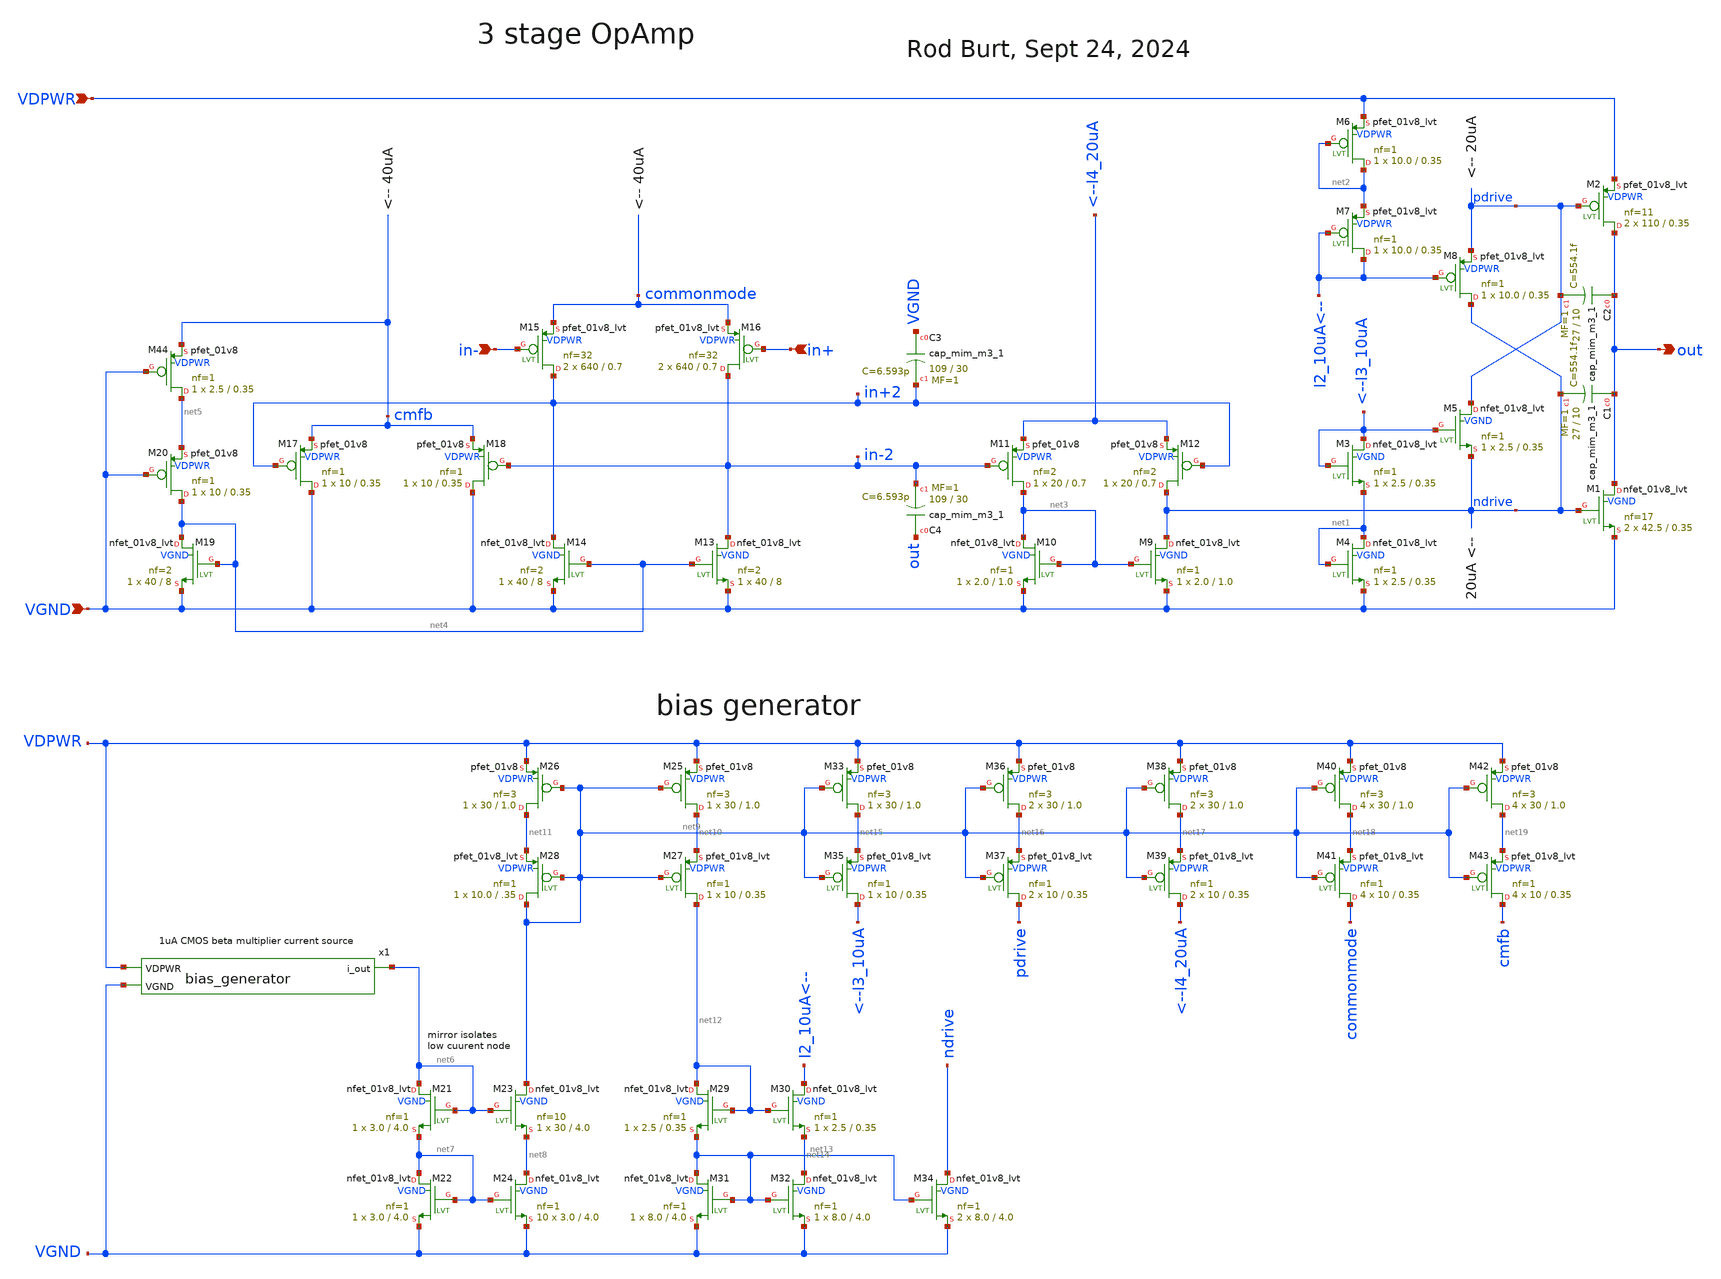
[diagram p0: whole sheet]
** sch_path: xschem/op_amp_3stage.sch
**.subckt op_amp_3stage out VDPWR VGND in- in+
*.opin out
*.ipin VDPWR
*.ipin VGND
*.ipin in-
*.ipin in+
XM2 out pdrive VDPWR VDPWR sky130_fd_pr__pfet_01v8_lvt L=0.35 W=110 nf=11 ad='int((nf+1)/2) * W/nf * 0.29'
+ as='int((nf+2)/2) * W/nf * 0.29' pd='2*int((nf+1)/2) * (W/nf + 0.29)' ps='2*int((nf+2)/2) * (W/nf + 0.29)'
+ nrd='0.29 / W' nrs='0.29 / W' sa=0 sb=0 sd=0 mult=2 m=2
XM6 net2 net2 VDPWR VDPWR sky130_fd_pr__pfet_01v8_lvt L=0.35 W=10.0 nf=1 ad='int((nf+1)/2) * W/nf * 0.29'
+ as='int((nf+2)/2) * W/nf * 0.29' pd='2*int((nf+1)/2) * (W/nf + 0.29)' ps='2*int((nf+2)/2) * (W/nf + 0.29)'
+ nrd='0.29 / W' nrs='0.29 / W' sa=0 sb=0 sd=0 mult=1 m=1
XM8 ndrive I2_10uA<-- pdrive VDPWR sky130_fd_pr__pfet_01v8_lvt L=0.35 W=10.0 nf=1 ad='int((nf+1)/2) * W/nf * 0.29'
+ as='int((nf+2)/2) * W/nf * 0.29' pd='2*int((nf+1)/2) * (W/nf + 0.29)' ps='2*int((nf+2)/2) * (W/nf + 0.29)'
+ nrd='0.29 / W' nrs='0.29 / W' sa=0 sb=0 sd=0 mult=1 m=1
XM7 I2_10uA<-- I2_10uA<-- net2 VDPWR sky130_fd_pr__pfet_01v8_lvt L=0.35 W=10.0 nf=1 ad='int((nf+1)/2) * W/nf * 0.29'
+ as='int((nf+2)/2) * W/nf * 0.29' pd='2*int((nf+1)/2) * (W/nf + 0.29)' ps='2*int((nf+2)/2) * (W/nf + 0.29)'
+ nrd='0.29 / W' nrs='0.29 / W' sa=0 sb=0 sd=0 mult=1 m=1
XM3 <--I3_10uA <--I3_10uA net1 VGND sky130_fd_pr__nfet_01v8_lvt L=0.35 W=2.5 nf=1 ad='int((nf+1)/2) * W/nf * 0.29'
+ as='int((nf+2)/2) * W/nf * 0.29' pd='2*int((nf+1)/2) * (W/nf + 0.29)' ps='2*int((nf+2)/2) * (W/nf + 0.29)'
+ nrd='0.29 / W' nrs='0.29 / W' sa=0 sb=0 sd=0 mult=1 m=1
M5 pdrive <--I3_10uA ndrive VGND sky130_fd_pr__nfet_01v8_lvt L=0.35 W=2.5 nf=1 ad='int((nf+1)/2) * W/nf * 0.29'
+ as='int((nf+2)/2) * W/nf * 0.29' pd='2*int((nf+1)/2) * (W/nf + 0.29)' ps='2*int((nf+2)/2) * (W/nf + 0.29)'
+ nrd='0.29 / W' nrs='0.29 / W' sa=0 sb=0 sd=0 mult=1 m=1
XM4 net1 net1 VGND VGND sky130_fd_pr__nfet_01v8_lvt L=0.35 W=2.5 nf=1 ad='int((nf+1)/2) * W/nf * 0.29'
+ as='int((nf+2)/2) * W/nf * 0.29' pd='2*int((nf+1)/2) * (W/nf + 0.29)' ps='2*int((nf+2)/2) * (W/nf + 0.29)'
+ nrd='0.29 / W' nrs='0.29 / W' sa=0 sb=0 sd=0 mult=1 m=1
XM1 out ndrive VGND VGND sky130_fd_pr__nfet_01v8_lvt L=0.35 W=42.5 nf=17 ad='int((nf+1)/2) * W/nf * 0.29'
+ as='int((nf+2)/2) * W/nf * 0.29' pd='2*int((nf+1)/2) * (W/nf + 0.29)' ps='2*int((nf+2)/2) * (W/nf + 0.29)'
+ nrd='0.29 / W' nrs='0.29 / W' sa=0 sb=0 sd=0 mult=2 m=2
XM9 ndrive net3 VGND VGND sky130_fd_pr__nfet_01v8_lvt L=1.0 W=2.0 nf=1 ad='int((nf+1)/2) * W/nf * 0.29'
+ as='int((nf+2)/2) * W/nf * 0.29' pd='2*int((nf+1)/2) * (W/nf + 0.29)' ps='2*int((nf+2)/2) * (W/nf + 0.29)'
+ nrd='0.29 / W' nrs='0.29 / W' sa=0 sb=0 sd=0 mult=1 m=1
XM10 net3 net3 VGND VGND sky130_fd_pr__nfet_01v8_lvt L=1.0 W=2.0 nf=1 ad='int((nf+1)/2) * W/nf * 0.29'
+ as='int((nf+2)/2) * W/nf * 0.29' pd='2*int((nf+1)/2) * (W/nf + 0.29)' ps='2*int((nf+2)/2) * (W/nf + 0.29)'
+ nrd='0.29 / W' nrs='0.29 / W' sa=0 sb=0 sd=0 mult=1 m=1
XM11 net3 in-2 <--I4_20uA VDPWR sky130_fd_pr__pfet_01v8 L=0.7 W=20 nf=2 ad='int((nf+1)/2) * W/nf * 0.29'
+ as='int((nf+2)/2) * W/nf * 0.29' pd='2*int((nf+1)/2) * (W/nf + 0.29)' ps='2*int((nf+2)/2) * (W/nf + 0.29)'
+ nrd='0.29 / W' nrs='0.29 / W' sa=0 sb=0 sd=0 mult=1 m=1
XM12 ndrive in+2 <--I4_20uA VDPWR sky130_fd_pr__pfet_01v8 L=0.7 W=20 nf=2 ad='int((nf+1)/2) * W/nf * 0.29'
+ as='int((nf+2)/2) * W/nf * 0.29' pd='2*int((nf+1)/2) * (W/nf + 0.29)' ps='2*int((nf+2)/2) * (W/nf + 0.29)'
+ nrd='0.29 / W' nrs='0.29 / W' sa=0 sb=0 sd=0 mult=1 m=1
XC1 out ndrive sky130_fd_pr__cap_mim_m3_1 W=27 L=10 MF=1 m=1
XC2 out pdrive sky130_fd_pr__cap_mim_m3_1 W=27 L=10 MF=1 m=1
XM13 in-2 net4 VGND VGND sky130_fd_pr__nfet_01v8_lvt L=8 W=40 nf=2 ad='int((nf+1)/2) * W/nf * 0.29' as='int((nf+2)/2) * W/nf * 0.29'
+ pd='2*int((nf+1)/2) * (W/nf + 0.29)' ps='2*int((nf+2)/2) * (W/nf + 0.29)' nrd='0.29 / W' nrs='0.29 / W'
+ sa=0 sb=0 sd=0 mult=1 m=1
XM14 in+2 net4 VGND VGND sky130_fd_pr__nfet_01v8_lvt L=8 W=40 nf=2 ad='int((nf+1)/2) * W/nf * 0.29' as='int((nf+2)/2) * W/nf * 0.29'
+ pd='2*int((nf+1)/2) * (W/nf + 0.29)' ps='2*int((nf+2)/2) * (W/nf + 0.29)' nrd='0.29 / W' nrs='0.29 / W'
+ sa=0 sb=0 sd=0 mult=1 m=1
XC3 VGND in+2 sky130_fd_pr__cap_mim_m3_1 W=109 L=30 MF=1 m=1
XC4 out in-2 sky130_fd_pr__cap_mim_m3_1 W=109 L=30 MF=1 m=1
XM15 in+2 in- commonmode VDPWR sky130_fd_pr__pfet_01v8_lvt L=0.7 W=640 nf=32 ad='int((nf+1)/2) * W/nf * 0.29'
+ as='int((nf+2)/2) * W/nf * 0.29' pd='2*int((nf+1)/2) * (W/nf + 0.29)' ps='2*int((nf+2)/2) * (W/nf + 0.29)'
+ nrd='0.29 / W' nrs='0.29 / W' sa=0 sb=0 sd=0 mult=2 m=2
XM16 in-2 in+ commonmode VDPWR sky130_fd_pr__pfet_01v8_lvt L=0.7 W=640 nf=32 ad='int((nf+1)/2) * W/nf * 0.29'
+ as='int((nf+2)/2) * W/nf * 0.29' pd='2*int((nf+1)/2) * (W/nf + 0.29)' ps='2*int((nf+2)/2) * (W/nf + 0.29)'
+ nrd='0.29 / W' nrs='0.29 / W' sa=0 sb=0 sd=0 mult=2 m=2
XM19 net4 net4 VGND VGND sky130_fd_pr__nfet_01v8_lvt L=8 W=40 nf=2 ad='int((nf+1)/2) * W/nf * 0.29' as='int((nf+2)/2) * W/nf * 0.29'
+ pd='2*int((nf+1)/2) * (W/nf + 0.29)' ps='2*int((nf+2)/2) * (W/nf + 0.29)' nrd='0.29 / W' nrs='0.29 / W'
+ sa=0 sb=0 sd=0 mult=1 m=1
XM20 net4 VGND net5 VDPWR sky130_fd_pr__pfet_01v8 L=0.35 W=10 nf=1 ad='int((nf+1)/2) * W/nf * 0.29' as='int((nf+2)/2) * W/nf * 0.29'
+ pd='2*int((nf+1)/2) * (W/nf + 0.29)' ps='2*int((nf+2)/2) * (W/nf + 0.29)' nrd='0.29 / W' nrs='0.29 / W'
+ sa=0 sb=0 sd=0 mult=1 m=1
XM17 VGND in+2 cmfb VDPWR sky130_fd_pr__pfet_01v8 L=0.35 W=10 nf=1 ad='int((nf+1)/2) * W/nf * 0.29' as='int((nf+2)/2) * W/nf * 0.29'
+ pd='2*int((nf+1)/2) * (W/nf + 0.29)' ps='2*int((nf+2)/2) * (W/nf + 0.29)' nrd='0.29 / W' nrs='0.29 / W'
+ sa=0 sb=0 sd=0 mult=1 m=1
XM18 VGND in-2 cmfb VDPWR sky130_fd_pr__pfet_01v8 L=0.35 W=10 nf=1 ad='int((nf+1)/2) * W/nf * 0.29' as='int((nf+2)/2) * W/nf * 0.29'
+ pd='2*int((nf+1)/2) * (W/nf + 0.29)' ps='2*int((nf+2)/2) * (W/nf + 0.29)' nrd='0.29 / W' nrs='0.29 / W'
+ sa=0 sb=0 sd=0 mult=1 m=1
x1 VDPWR net6 VGND bias_generator
XM21 net6 net6 net7 VGND sky130_fd_pr__nfet_01v8_lvt L=4.0 W=3.0 nf=1 ad='int((nf+1)/2) * W/nf * 0.29'
+ as='int((nf+2)/2) * W/nf * 0.29' pd='2*int((nf+1)/2) * (W/nf + 0.29)' ps='2*int((nf+2)/2) * (W/nf + 0.29)'
+ nrd='0.29 / W' nrs='0.29 / W' sa=0 sb=0 sd=0 mult=1 m=1
XM23 net9 net6 net8 VGND sky130_fd_pr__nfet_01v8_lvt L=4.0 W=30 nf=10 ad='int((nf+1)/2) * W/nf * 0.29'
+ as='int((nf+2)/2) * W/nf * 0.29' pd='2*int((nf+1)/2) * (W/nf + 0.29)' ps='2*int((nf+2)/2) * (W/nf + 0.29)'
+ nrd='0.29 / W' nrs='0.29 / W' sa=0 sb=0 sd=0 mult=1 m=1
XM25 net10 net9 VDPWR VDPWR sky130_fd_pr__pfet_01v8 L=1.0 W=30 nf=3 ad='int((nf+1)/2) * W/nf * 0.29'
+ as='int((nf+2)/2) * W/nf * 0.29' pd='2*int((nf+1)/2) * (W/nf + 0.29)' ps='2*int((nf+2)/2) * (W/nf + 0.29)'
+ nrd='0.29 / W' nrs='0.29 / W' sa=0 sb=0 sd=0 mult=1 m=1
XM26 net11 net9 VDPWR VDPWR sky130_fd_pr__pfet_01v8 L=1.0 W=30 nf=3 ad='int((nf+1)/2) * W/nf * 0.29'
+ as='int((nf+2)/2) * W/nf * 0.29' pd='2*int((nf+1)/2) * (W/nf + 0.29)' ps='2*int((nf+2)/2) * (W/nf + 0.29)'
+ nrd='0.29 / W' nrs='0.29 / W' sa=0 sb=0 sd=0 mult=1 m=1
XM27 net12 net9 net10 VDPWR sky130_fd_pr__pfet_01v8_lvt L=0.35 W=10 nf=1 ad='int((nf+1)/2) * W/nf * 0.29'
+ as='int((nf+2)/2) * W/nf * 0.29' pd='2*int((nf+1)/2) * (W/nf + 0.29)' ps='2*int((nf+2)/2) * (W/nf + 0.29)'
+ nrd='0.29 / W' nrs='0.29 / W' sa=0 sb=0 sd=0 mult=1 m=1
XM28 net9 net9 net11 VDPWR sky130_fd_pr__pfet_01v8_lvt L=.35 W=10.0 nf=1 ad='int((nf+1)/2) * W/nf * 0.29'
+ as='int((nf+2)/2) * W/nf * 0.29' pd='2*int((nf+1)/2) * (W/nf + 0.29)' ps='2*int((nf+2)/2) * (W/nf + 0.29)'
+ nrd='0.29 / W' nrs='0.29 / W' sa=0 sb=0 sd=0 mult=1 m=1
XM22 net7 net7 VGND VGND sky130_fd_pr__nfet_01v8_lvt L=4.0 W=3.0 nf=1 ad='int((nf+1)/2) * W/nf * 0.29'
+ as='int((nf+2)/2) * W/nf * 0.29' pd='2*int((nf+1)/2) * (W/nf + 0.29)' ps='2*int((nf+2)/2) * (W/nf + 0.29)'
+ nrd='0.29 / W' nrs='0.29 / W' sa=0 sb=0 sd=0 mult=1 m=1
XM24 net8 net7 VGND VGND sky130_fd_pr__nfet_01v8_lvt L=4.0 W=3.0 nf=1 ad='int((nf+1)/2) * W/nf * 0.29'
+ as='int((nf+2)/2) * W/nf * 0.29' pd='2*int((nf+1)/2) * (W/nf + 0.29)' ps='2*int((nf+2)/2) * (W/nf + 0.29)'
+ nrd='0.29 / W' nrs='0.29 / W' sa=0 sb=0 sd=0 mult=10 m=10
XM29 net12 net12 net13 VGND sky130_fd_pr__nfet_01v8_lvt L=0.35 W=2.5 nf=1 ad='int((nf+1)/2) * W/nf * 0.29'
+ as='int((nf+2)/2) * W/nf * 0.29' pd='2*int((nf+1)/2) * (W/nf + 0.29)' ps='2*int((nf+2)/2) * (W/nf + 0.29)'
+ nrd='0.29 / W' nrs='0.29 / W' sa=0 sb=0 sd=0 mult=1 m=1
XM30 I2_10uA<-- net12 net14 VGND sky130_fd_pr__nfet_01v8_lvt L=0.35 W=2.5 nf=1 ad='int((nf+1)/2) * W/nf * 0.29'
+ as='int((nf+2)/2) * W/nf * 0.29' pd='2*int((nf+1)/2) * (W/nf + 0.29)' ps='2*int((nf+2)/2) * (W/nf + 0.29)'
+ nrd='0.29 / W' nrs='0.29 / W' sa=0 sb=0 sd=0 mult=1 m=1
XM31 net13 net13 VGND VGND sky130_fd_pr__nfet_01v8_lvt L=4.0 W=8.0 nf=1 ad='int((nf+1)/2) * W/nf * 0.29'
+ as='int((nf+2)/2) * W/nf * 0.29' pd='2*int((nf+1)/2) * (W/nf + 0.29)' ps='2*int((nf+2)/2) * (W/nf + 0.29)'
+ nrd='0.29 / W' nrs='0.29 / W' sa=0 sb=0 sd=0 mult=1 m=1
XM32 net14 net13 VGND VGND sky130_fd_pr__nfet_01v8_lvt L=4.0 W=8.0 nf=1 ad='int((nf+1)/2) * W/nf * 0.29'
+ as='int((nf+2)/2) * W/nf * 0.29' pd='2*int((nf+1)/2) * (W/nf + 0.29)' ps='2*int((nf+2)/2) * (W/nf + 0.29)'
+ nrd='0.29 / W' nrs='0.29 / W' sa=0 sb=0 sd=0 mult=1 m=1
XM34 ndrive net13 VGND VGND sky130_fd_pr__nfet_01v8_lvt L=4.0 W=8.0 nf=1 ad='int((nf+1)/2) * W/nf * 0.29'
+ as='int((nf+2)/2) * W/nf * 0.29' pd='2*int((nf+1)/2) * (W/nf + 0.29)' ps='2*int((nf+2)/2) * (W/nf + 0.29)'
+ nrd='0.29 / W' nrs='0.29 / W' sa=0 sb=0 sd=0 mult=2 m=2
XM33 net15 net9 VDPWR VDPWR sky130_fd_pr__pfet_01v8 L=1.0 W=30 nf=3 ad='int((nf+1)/2) * W/nf * 0.29'
+ as='int((nf+2)/2) * W/nf * 0.29' pd='2*int((nf+1)/2) * (W/nf + 0.29)' ps='2*int((nf+2)/2) * (W/nf + 0.29)'
+ nrd='0.29 / W' nrs='0.29 / W' sa=0 sb=0 sd=0 mult=1 m=1
XM35 <--I3_10uA net9 net15 VDPWR sky130_fd_pr__pfet_01v8_lvt L=0.35 W=10 nf=1 ad='int((nf+1)/2) * W/nf * 0.29'
+ as='int((nf+2)/2) * W/nf * 0.29' pd='2*int((nf+1)/2) * (W/nf + 0.29)' ps='2*int((nf+2)/2) * (W/nf + 0.29)'
+ nrd='0.29 / W' nrs='0.29 / W' sa=0 sb=0 sd=0 mult=1 m=1
XM36 net16 net9 VDPWR VDPWR sky130_fd_pr__pfet_01v8 L=1.0 W=30 nf=3 ad='int((nf+1)/2) * W/nf * 0.29'
+ as='int((nf+2)/2) * W/nf * 0.29' pd='2*int((nf+1)/2) * (W/nf + 0.29)' ps='2*int((nf+2)/2) * (W/nf + 0.29)'
+ nrd='0.29 / W' nrs='0.29 / W' sa=0 sb=0 sd=0 mult=2 m=2
XM37 pdrive net9 net16 VDPWR sky130_fd_pr__pfet_01v8_lvt L=0.35 W=10 nf=1 ad='int((nf+1)/2) * W/nf * 0.29'
+ as='int((nf+2)/2) * W/nf * 0.29' pd='2*int((nf+1)/2) * (W/nf + 0.29)' ps='2*int((nf+2)/2) * (W/nf + 0.29)'
+ nrd='0.29 / W' nrs='0.29 / W' sa=0 sb=0 sd=0 mult=2 m=2
XM38 net17 net9 VDPWR VDPWR sky130_fd_pr__pfet_01v8 L=1.0 W=30 nf=3 ad='int((nf+1)/2) * W/nf * 0.29'
+ as='int((nf+2)/2) * W/nf * 0.29' pd='2*int((nf+1)/2) * (W/nf + 0.29)' ps='2*int((nf+2)/2) * (W/nf + 0.29)'
+ nrd='0.29 / W' nrs='0.29 / W' sa=0 sb=0 sd=0 mult=2 m=2
XM39 <--I4_20uA net9 net17 VDPWR sky130_fd_pr__pfet_01v8_lvt L=0.35 W=10 nf=1 ad='int((nf+1)/2) * W/nf * 0.29'
+ as='int((nf+2)/2) * W/nf * 0.29' pd='2*int((nf+1)/2) * (W/nf + 0.29)' ps='2*int((nf+2)/2) * (W/nf + 0.29)'
+ nrd='0.29 / W' nrs='0.29 / W' sa=0 sb=0 sd=0 mult=2 m=2
XM40 net18 net9 VDPWR VDPWR sky130_fd_pr__pfet_01v8 L=1.0 W=30 nf=3 ad='int((nf+1)/2) * W/nf * 0.29'
+ as='int((nf+2)/2) * W/nf * 0.29' pd='2*int((nf+1)/2) * (W/nf + 0.29)' ps='2*int((nf+2)/2) * (W/nf + 0.29)'
+ nrd='0.29 / W' nrs='0.29 / W' sa=0 sb=0 sd=0 mult=4 m=4
XM41 commonmode net9 net18 VDPWR sky130_fd_pr__pfet_01v8_lvt L=0.35 W=10 nf=1 ad='int((nf+1)/2) * W/nf * 0.29'
+ as='int((nf+2)/2) * W/nf * 0.29' pd='2*int((nf+1)/2) * (W/nf + 0.29)' ps='2*int((nf+2)/2) * (W/nf + 0.29)'
+ nrd='0.29 / W' nrs='0.29 / W' sa=0 sb=0 sd=0 mult=4 m=4
XM42 net19 net9 VDPWR VDPWR sky130_fd_pr__pfet_01v8 L=1.0 W=30 nf=3 ad='int((nf+1)/2) * W/nf * 0.29'
+ as='int((nf+2)/2) * W/nf * 0.29' pd='2*int((nf+1)/2) * (W/nf + 0.29)' ps='2*int((nf+2)/2) * (W/nf + 0.29)'
+ nrd='0.29 / W' nrs='0.29 / W' sa=0 sb=0 sd=0 mult=4 m=4
XM43 cmfb net9 net19 VDPWR sky130_fd_pr__pfet_01v8_lvt L=0.35 W=10 nf=1 ad='int((nf+1)/2) * W/nf * 0.29'
+ as='int((nf+2)/2) * W/nf * 0.29' pd='2*int((nf+1)/2) * (W/nf + 0.29)' ps='2*int((nf+2)/2) * (W/nf + 0.29)'
+ nrd='0.29 / W' nrs='0.29 / W' sa=0 sb=0 sd=0 mult=4 m=4
XM44 net5 VGND cmfb VDPWR sky130_fd_pr__pfet_01v8 L=0.35 W=2.5 nf=1 ad='int((nf+1)/2) * W/nf * 0.29'
+ as='int((nf+2)/2) * W/nf * 0.29' pd='2*int((nf+1)/2) * (W/nf + 0.29)' ps='2*int((nf+2)/2) * (W/nf + 0.29)'
+ nrd='0.29 / W' nrs='0.29 / W' sa=0 sb=0 sd=0 mult=1 m=1
**.ends

* expanding   symbol:  /foss/designs/tt09-analog-opamp-3stage/xschem/bias_generator.sym # of pins=3
** sym_path: xschem/bias_generator.sym
** sch_path: xschem/bias_generator.sch
.subckt bias_generator VDPWR i_out VGND
*.ipin VGND
*.ipin VDPWR
*.opin i_out
XM9 ncascode ncascode net1 VGND sky130_fd_pr__nfet_01v8_lvt L=1.0 W=8.0 nf=1 ad='int((nf+1)/2) * W/nf * 0.29'
+ as='int((nf+2)/2) * W/nf * 0.29' pd='2*int((nf+1)/2) * (W/nf + 0.29)' ps='2*int((nf+2)/2) * (W/nf + 0.29)'
+ nrd='0.29 / W' nrs='0.29 / W' sa=0 sb=0 sd=0 mult=1 m=1
XM10 pgate ncascode net4 VGND sky130_fd_pr__nfet_01v8_lvt L=1.0 W=8.0 nf=1 ad='int((nf+1)/2) * W/nf * 0.29'
+ as='int((nf+2)/2) * W/nf * 0.29' pd='2*int((nf+1)/2) * (W/nf + 0.29)' ps='2*int((nf+2)/2) * (W/nf + 0.29)'
+ nrd='0.29 / W' nrs='0.29 / W' sa=0 sb=0 sd=0 mult=1 m=1
XM2 net4 net1 ptat VGND sky130_fd_pr__nfet_01v8 L=1.0 W=8.0 nf=1 ad='int((nf+1)/2) * W/nf * 0.29' as='int((nf+2)/2) * W/nf * 0.29'
+ pd='2*int((nf+1)/2) * (W/nf + 0.29)' ps='2*int((nf+2)/2) * (W/nf + 0.29)' nrd='0.29 / W' nrs='0.29 / W'
+ sa=0 sb=0 sd=0 mult=8 m=8
XM18 pgate startup VGND VGND sky130_fd_pr__nfet_01v8 L=8.0 W=0.42 nf=1 ad='int((nf+1)/2) * W/nf * 0.29'
+ as='int((nf+2)/2) * W/nf * 0.29' pd='2*int((nf+1)/2) * (W/nf + 0.29)' ps='2*int((nf+2)/2) * (W/nf + 0.29)'
+ nrd='0.29 / W' nrs='0.29 / W' sa=0 sb=0 sd=0 mult=1 m=1
XM17 startup net1 VGND VGND sky130_fd_pr__nfet_01v8 L=1.0 W=8.0 nf=1 ad='int((nf+1)/2) * W/nf * 0.29'
+ as='int((nf+2)/2) * W/nf * 0.29' pd='2*int((nf+1)/2) * (W/nf + 0.29)' ps='2*int((nf+2)/2) * (W/nf + 0.29)'
+ nrd='0.29 / W' nrs='0.29 / W' sa=0 sb=0 sd=0 mult=1 m=1
XM1 net1 net1 VGND VGND sky130_fd_pr__nfet_01v8 L=1.0 W=8.0 nf=1 ad='int((nf+1)/2) * W/nf * 0.29' as='int((nf+2)/2) * W/nf * 0.29'
+ pd='2*int((nf+1)/2) * (W/nf + 0.29)' ps='2*int((nf+2)/2) * (W/nf + 0.29)' nrd='0.29 / W' nrs='0.29 / W'
+ sa=0 sb=0 sd=0 mult=1 m=1
XM5 ptat drive VGND VGND sky130_fd_pr__nfet_01v8 L=8.0 W=1.0 nf=1 ad='int((nf+1)/2) * W/nf * 0.29' as='int((nf+2)/2) * W/nf * 0.29'
+ pd='2*int((nf+1)/2) * (W/nf + 0.29)' ps='2*int((nf+2)/2) * (W/nf + 0.29)' nrd='0.29 / W' nrs='0.29 / W'
+ sa=0 sb=0 sd=0 mult=2 m=2
XM7 drive drive net3 VGND sky130_fd_pr__nfet_01v8 L=13.1 W=1.0 nf=1 ad='int((nf+1)/2) * W/nf * 0.29'
+ as='int((nf+2)/2) * W/nf * 0.29' pd='2*int((nf+1)/2) * (W/nf + 0.29)' ps='2*int((nf+2)/2) * (W/nf + 0.29)'
+ nrd='0.29 / W' nrs='0.29 / W' sa=0 sb=0 sd=0 mult=1 m=1
XM8 net3 drive ptat VGND sky130_fd_pr__nfet_01v8 L=8.0 W=1.0 nf=1 ad='int((nf+1)/2) * W/nf * 0.29' as='int((nf+2)/2) * W/nf * 0.29'
+ pd='2*int((nf+1)/2) * (W/nf + 0.29)' ps='2*int((nf+2)/2) * (W/nf + 0.29)' nrd='0.29 / W' nrs='0.29 / W'
+ sa=0 sb=0 sd=0 mult=1 m=1
XM4 net2 pgate VDPWR VDPWR sky130_fd_pr__pfet_01v8 L=1.0 W=8.0 nf=1 ad='int((nf+1)/2) * W/nf * 0.29'
+ as='int((nf+2)/2) * W/nf * 0.29' pd='2*int((nf+1)/2) * (W/nf + 0.29)' ps='2*int((nf+2)/2) * (W/nf + 0.29)'
+ nrd='0.29 / W' nrs='0.29 / W' sa=0 sb=0 sd=0 mult=1 m=1
XM6 net6 pgate VDPWR VDPWR sky130_fd_pr__pfet_01v8 L=1.0 W=8.0 nf=1 ad='int((nf+1)/2) * W/nf * 0.29'
+ as='int((nf+2)/2) * W/nf * 0.29' pd='2*int((nf+1)/2) * (W/nf + 0.29)' ps='2*int((nf+2)/2) * (W/nf + 0.29)'
+ nrd='0.29 / W' nrs='0.29 / W' sa=0 sb=0 sd=0 mult=1 m=1
XM14 net7 pgate VDPWR VDPWR sky130_fd_pr__pfet_01v8 L=1.0 W=8.0 nf=1 ad='int((nf+1)/2) * W/nf * 0.29'
+ as='int((nf+2)/2) * W/nf * 0.29' pd='2*int((nf+1)/2) * (W/nf + 0.29)' ps='2*int((nf+2)/2) * (W/nf + 0.29)'
+ nrd='0.29 / W' nrs='0.29 / W' sa=0 sb=0 sd=0 mult=1 m=1
XM3 net5 pgate VDPWR VDPWR sky130_fd_pr__pfet_01v8 L=1.0 W=8.0 nf=1 ad='int((nf+1)/2) * W/nf * 0.29'
+ as='int((nf+2)/2) * W/nf * 0.29' pd='2*int((nf+1)/2) * (W/nf + 0.29)' ps='2*int((nf+2)/2) * (W/nf + 0.29)'
+ nrd='0.29 / W' nrs='0.29 / W' sa=0 sb=0 sd=0 mult=1 m=1
XM16 startup net1 VDPWR VDPWR sky130_fd_pr__pfet_01v8 L=8.0 W=0.42 nf=1 ad='int((nf+1)/2) * W/nf * 0.29'
+ as='int((nf+2)/2) * W/nf * 0.29' pd='2*int((nf+1)/2) * (W/nf + 0.29)' ps='2*int((nf+2)/2) * (W/nf + 0.29)'
+ nrd='0.29 / W' nrs='0.29 / W' sa=0 sb=0 sd=0 mult=1 m=1
XM12 pgate pgate net2 VDPWR sky130_fd_pr__pfet_01v8_lvt L=1.0 W=8.0 nf=1 ad='int((nf+1)/2) * W/nf * 0.29'
+ as='int((nf+2)/2) * W/nf * 0.29' pd='2*int((nf+1)/2) * (W/nf + 0.29)' ps='2*int((nf+2)/2) * (W/nf + 0.29)'
+ nrd='0.29 / W' nrs='0.29 / W' sa=0 sb=0 sd=0 mult=1 m=1
XM13 drive pgate net6 VDPWR sky130_fd_pr__pfet_01v8_lvt L=1.0 W=8.0 nf=1 ad='int((nf+1)/2) * W/nf * 0.29'
+ as='int((nf+2)/2) * W/nf * 0.29' pd='2*int((nf+1)/2) * (W/nf + 0.29)' ps='2*int((nf+2)/2) * (W/nf + 0.29)'
+ nrd='0.29 / W' nrs='0.29 / W' sa=0 sb=0 sd=0 mult=1 m=1
XM15 i_out pgate net7 VDPWR sky130_fd_pr__pfet_01v8_lvt L=1.0 W=8.0 nf=1 ad='int((nf+1)/2) * W/nf * 0.29'
+ as='int((nf+2)/2) * W/nf * 0.29' pd='2*int((nf+1)/2) * (W/nf + 0.29)' ps='2*int((nf+2)/2) * (W/nf + 0.29)'
+ nrd='0.29 / W' nrs='0.29 / W' sa=0 sb=0 sd=0 mult=1 m=1
XM11 ncascode pgate net5 VDPWR sky130_fd_pr__pfet_01v8_lvt L=1.0 W=8.0 nf=1 ad='int((nf+1)/2) * W/nf * 0.29'
+ as='int((nf+2)/2) * W/nf * 0.29' pd='2*int((nf+1)/2) * (W/nf + 0.29)' ps='2*int((nf+2)/2) * (W/nf + 0.29)'
+ nrd='0.29 / W' nrs='0.29 / W' sa=0 sb=0 sd=0 mult=1 m=1
.ends

.end
